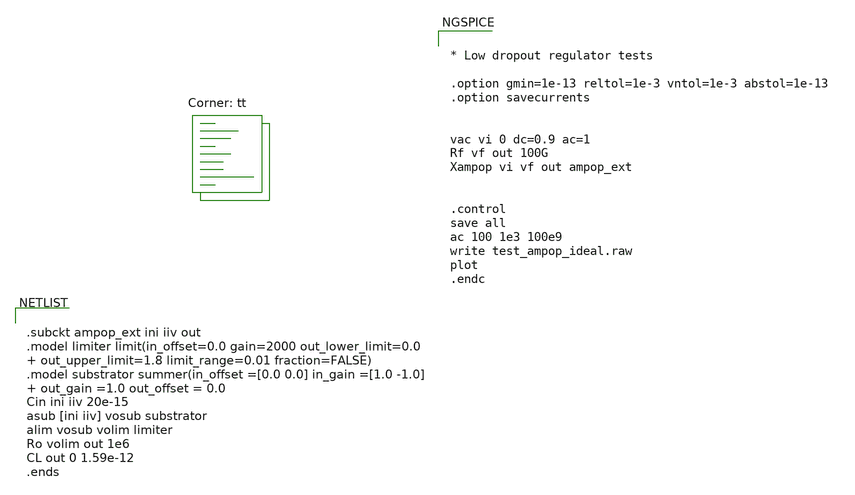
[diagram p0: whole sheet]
** sch_path: xschem/untitled.sch
**.subckt untitled
**** begin user architecture code


.subckt ampop_ext ini iiv out
.model limiter limit(in_offset=0.0 gain=2000 out_lower_limit=0.0  out_upper_limit=1.8
+ limit_range=0.01 fraction=FALSE)
.model substrator summer(in_offset =[0.0 0.0] in_gain =[1.0 -1.0]  out_gain =1.0 out_offset = 0.0
Cin ini iiv 20e-15
asub [ini iiv] vosub substrator
alim vosub volim limiter
Ro volim out 1e6
CL out 0 1.59e-12
.ends




* Low dropout regulator tests

.option gmin=1e-13 reltol=1e-3 vntol=1e-3 abstol=1e-13
.option savecurrents


vac vi 0 dc=0.9 ac=1
Rf vf out 100G
Xampop vi vf out ampop_ext


.control
save all
ac 100 1e3 100e9
write test_ampop_ideal.raw
plot
.endc


.lib $::SKYWATER_MODELS/sky130.lib.spice tt
**** end user architecture code
**.ends
.end
